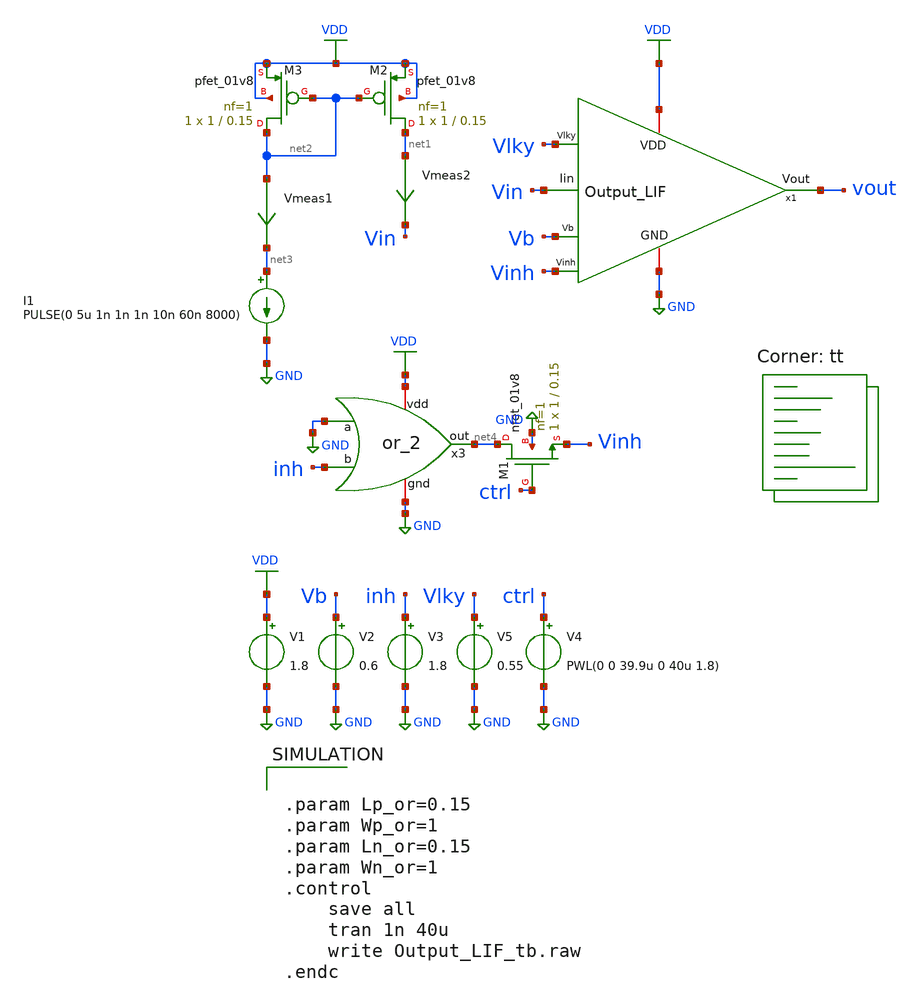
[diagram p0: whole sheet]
** sch_path: SNN/Output_LIF_tb.sch
**.subckt Output_LIF_tb
V1 VDD GND 1.8
V2 Vb GND 0.6
I1 net3 GND PULSE(0 5u 1n 1n 1n 10n 60n 8000)
XM2 net1 net2 VDD VDD sky130_fd_pr__pfet_01v8 L=0.15 W=1 nf=1 ad='int((nf+1)/2) * W/nf * 0.29' as='int((nf+2)/2) * W/nf * 0.29'
+ pd='2*int((nf+1)/2) * (W/nf + 0.29)' ps='2*int((nf+2)/2) * (W/nf + 0.29)' nrd='0.29 / W' nrs='0.29 / W'
+ sa=0 sb=0 sd=0 mult=1 m=1
XM3 net2 net2 VDD VDD sky130_fd_pr__pfet_01v8 L=0.15 W=1 nf=1 ad='int((nf+1)/2) * W/nf * 0.29' as='int((nf+2)/2) * W/nf * 0.29'
+ pd='2*int((nf+1)/2) * (W/nf + 0.29)' ps='2*int((nf+2)/2) * (W/nf + 0.29)' nrd='0.29 / W' nrs='0.29 / W'
+ sa=0 sb=0 sd=0 mult=1 m=1
Vmeas1 net2 net3 0
.save i(vmeas1)
Vmeas2 net1 Vin 0
.save i(vmeas2)
V4 ctrl GND PWL(0 0 39.9u 0 40u 1.8)
x3 VDD GND inh net4 GND or_2
XM1 net4 ctrl Vinh GND sky130_fd_pr__nfet_01v8 L=0.15 W=1 nf=1 ad='int((nf+1)/2) * W/nf * 0.29' as='int((nf+2)/2) * W/nf * 0.29'
+ pd='2*int((nf+1)/2) * (W/nf + 0.29)' ps='2*int((nf+2)/2) * (W/nf + 0.29)' nrd='0.29 / W' nrs='0.29 / W'
+ sa=0 sb=0 sd=0 mult=1 m=1
V3 inh GND 1.8
V5 Vlky GND 0.55
x1 Vinh Vlky Vb VDD vout GND Vin Output_LIF
**** begin user architecture code


.param Lp_or=0.15
.param Wp_or=1
.param Ln_or=0.15
.param Wn_or=1
.control
	save all
	tran 1n 40u
	write Output_LIF_tb.raw
.endc


.lib $::SKYWATER_MODELS/sky130.lib.spice tt
**** end user architecture code
**.ends

* expanding   symbol:  /home/ricardo/RATT_repos/Proyectos_xschem/inhibitory/or_2.sym # of pins=5
** sym_path: inhibitory/or_2.sym
** sch_path: inhibitory/or_2.sch
.subckt or_2 vdd a b out gnd
*.iopin gnd
*.ipin a
*.ipin b
*.opin out
*.iopin vdd
XM1 net1 a vdd vdd sky130_fd_pr__pfet_01v8 L={Lp_or} W={Wp_or} nf=1 ad='int((nf+1)/2) * W/nf * 0.29'
+ as='int((nf+2)/2) * W/nf * 0.29' pd='2*int((nf+1)/2) * (W/nf + 0.29)' ps='2*int((nf+2)/2) * (W/nf + 0.29)'
+ nrd='0.29 / W' nrs='0.29 / W' sa=0 sb=0 sd=0 mult=1 m=1
XM2 net2 b gnd gnd sky130_fd_pr__nfet_01v8 L={Ln_or} W={Wn_or} nf=1 ad='int((nf+1)/2) * W/nf * 0.29'
+ as='int((nf+2)/2) * W/nf * 0.29' pd='2*int((nf+1)/2) * (W/nf + 0.29)' ps='2*int((nf+2)/2) * (W/nf + 0.29)'
+ nrd='0.29 / W' nrs='0.29 / W' sa=0 sb=0 sd=0 mult=1 m=1
XM3 net2 b net1 vdd sky130_fd_pr__pfet_01v8 L={Lp_or} W={Wp_or} nf=1 ad='int((nf+1)/2) * W/nf * 0.29'
+ as='int((nf+2)/2) * W/nf * 0.29' pd='2*int((nf+1)/2) * (W/nf + 0.29)' ps='2*int((nf+2)/2) * (W/nf + 0.29)'
+ nrd='0.29 / W' nrs='0.29 / W' sa=0 sb=0 sd=0 mult=1 m=1
XM4 net2 a gnd gnd sky130_fd_pr__nfet_01v8 L={Ln_or} W={Wn_or} nf=1 ad='int((nf+1)/2) * W/nf * 0.29'
+ as='int((nf+2)/2) * W/nf * 0.29' pd='2*int((nf+1)/2) * (W/nf + 0.29)' ps='2*int((nf+2)/2) * (W/nf + 0.29)'
+ nrd='0.29 / W' nrs='0.29 / W' sa=0 sb=0 sd=0 mult=1 m=1
XM5 out net2 gnd gnd sky130_fd_pr__nfet_01v8 L={Ln_or} W={Wn_or} nf=1 ad='int((nf+1)/2) * W/nf * 0.29'
+ as='int((nf+2)/2) * W/nf * 0.29' pd='2*int((nf+1)/2) * (W/nf + 0.29)' ps='2*int((nf+2)/2) * (W/nf + 0.29)'
+ nrd='0.29 / W' nrs='0.29 / W' sa=0 sb=0 sd=0 mult=1 m=1
XM6 out net2 vdd vdd sky130_fd_pr__pfet_01v8 L={Lp_or} W={Wp_or} nf=1 ad='int((nf+1)/2) * W/nf * 0.29'
+ as='int((nf+2)/2) * W/nf * 0.29' pd='2*int((nf+1)/2) * (W/nf + 0.29)' ps='2*int((nf+2)/2) * (W/nf + 0.29)'
+ nrd='0.29 / W' nrs='0.29 / W' sa=0 sb=0 sd=0 mult=1 m=1
.ends


* expanding   symbol:  /home/ricardo/RATT_repos/Proyectos_xschem/SNN/Output_LIF.sym # of pins=7
** sym_path: Final_Design/Output_LIF.sym
** sch_path: Final_Design/Output_LIF.sch
.subckt Output_LIF Vinh Vlky Vb VDD Vout GND Iin
*.iopin GND
*.ipin Vb
*.iopin VDD
*.opin Vout
*.ipin Iin
*.ipin Vlky
*.ipin Vinh
XM5 net3 Vb GND GND sky130_fd_pr__nfet_01v8 L=0.5 W=5 nf=1 ad='int((nf+1)/2) * W/nf * 0.29' as='int((nf+2)/2) * W/nf * 0.29'
+ pd='2*int((nf+1)/2) * (W/nf + 0.29)' ps='2*int((nf+2)/2) * (W/nf + 0.29)' nrd='0.29 / W' nrs='0.29 / W'
+ sa=0 sb=0 sd=0 mult=1 m=1
XM4 net1 net2 net3 GND sky130_fd_pr__nfet_01v8 L=0.15 W=1.5 nf=1 ad='int((nf+1)/2) * W/nf * 0.29' as='int((nf+2)/2) * W/nf * 0.29'
+ pd='2*int((nf+1)/2) * (W/nf + 0.29)' ps='2*int((nf+2)/2) * (W/nf + 0.29)' nrd='0.29 / W' nrs='0.29 / W'
+ sa=0 sb=0 sd=0 mult=1 m=1
XM3 net1 net2 VDD VDD sky130_fd_pr__pfet_01v8 L=5 W=0.5 nf=1 ad='int((nf+1)/2) * W/nf * 0.29' as='int((nf+2)/2) * W/nf * 0.29'
+ pd='2*int((nf+1)/2) * (W/nf + 0.29)' ps='2*int((nf+2)/2) * (W/nf + 0.29)' nrd='0.29 / W' nrs='0.29 / W'
+ sa=0 sb=0 sd=0 mult=1 m=1
XC2 net1 GND sky130_fd_pr__cap_mim_m3_1 W=20 L=20 MF=1 m=1
XM2 Iin net1 GND GND sky130_fd_pr__nfet_01v8 L=0.5 W=5 nf=1 ad='int((nf+1)/2) * W/nf * 0.29' as='int((nf+2)/2) * W/nf * 0.29'
+ pd='2*int((nf+1)/2) * (W/nf + 0.29)' ps='2*int((nf+2)/2) * (W/nf + 0.29)' nrd='0.29 / W' nrs='0.29 / W'
+ sa=0 sb=0 sd=0 mult=1 m=1
XC1 Iin GND sky130_fd_pr__cap_mim_m3_1 W=20 L=10 MF=1 m=1
XM10 net4 Vout GND GND sky130_fd_pr__nfet_01v8 L=0.15 W=1.5 nf=1 ad='int((nf+1)/2) * W/nf * 0.29' as='int((nf+2)/2) * W/nf * 0.29'
+ pd='2*int((nf+1)/2) * (W/nf + 0.29)' ps='2*int((nf+2)/2) * (W/nf + 0.29)' nrd='0.29 / W' nrs='0.29 / W'
+ sa=0 sb=0 sd=0 mult=1 m=1
XM7 net2 Iin net4 GND sky130_fd_pr__nfet_01v8 L=0.15 W=1.5 nf=1 ad='int((nf+1)/2) * W/nf * 0.29' as='int((nf+2)/2) * W/nf * 0.29'
+ pd='2*int((nf+1)/2) * (W/nf + 0.29)' ps='2*int((nf+2)/2) * (W/nf + 0.29)' nrd='0.29 / W' nrs='0.29 / W'
+ sa=0 sb=0 sd=0 mult=1 m=1
XM6 net2 Iin VDD VDD sky130_fd_pr__pfet_01v8 L=0.15 W=1.5 nf=1 ad='int((nf+1)/2) * W/nf * 0.29' as='int((nf+2)/2) * W/nf * 0.29'
+ pd='2*int((nf+1)/2) * (W/nf + 0.29)' ps='2*int((nf+2)/2) * (W/nf + 0.29)' nrd='0.29 / W' nrs='0.29 / W'
+ sa=0 sb=0 sd=0 mult=1 m=1
XM9 Vout net2 net4 GND sky130_fd_pr__nfet_01v8 L=0.15 W=1.5 nf=1 ad='int((nf+1)/2) * W/nf * 0.29' as='int((nf+2)/2) * W/nf * 0.29'
+ pd='2*int((nf+1)/2) * (W/nf + 0.29)' ps='2*int((nf+2)/2) * (W/nf + 0.29)' nrd='0.29 / W' nrs='0.29 / W'
+ sa=0 sb=0 sd=0 mult=1 m=1
XM8 Vout net2 VDD VDD sky130_fd_pr__pfet_01v8 L=0.15 W=5 nf=1 ad='int((nf+1)/2) * W/nf * 0.29' as='int((nf+2)/2) * W/nf * 0.29'
+ pd='2*int((nf+1)/2) * (W/nf + 0.29)' ps='2*int((nf+2)/2) * (W/nf + 0.29)' nrd='0.29 / W' nrs='0.29 / W'
+ sa=0 sb=0 sd=0 mult=1 m=1
XM1 Iin Vlky GND GND sky130_fd_pr__nfet_01v8 L=0.15 W=1.5 nf=1 ad='int((nf+1)/2) * W/nf * 0.29' as='int((nf+2)/2) * W/nf * 0.29'
+ pd='2*int((nf+1)/2) * (W/nf + 0.29)' ps='2*int((nf+2)/2) * (W/nf + 0.29)' nrd='0.29 / W' nrs='0.29 / W'
+ sa=0 sb=0 sd=0 mult=1 m=1
XM11 VDD Vinh net1 GND sky130_fd_pr__nfet_01v8 L=0.15 W=1 nf=1 ad='int((nf+1)/2) * W/nf * 0.29' as='int((nf+2)/2) * W/nf * 0.29'
+ pd='2*int((nf+1)/2) * (W/nf + 0.29)' ps='2*int((nf+2)/2) * (W/nf + 0.29)' nrd='0.29 / W' nrs='0.29 / W'
+ sa=0 sb=0 sd=0 mult=1 m=1
.ends

.GLOBAL GND
.GLOBAL VDD
.end
